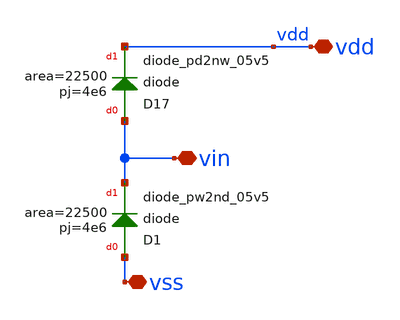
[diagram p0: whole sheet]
** sch_path: xschem/src/ESD/ESD.sch
**.subckt ESD vdd vin vss
*.iopin vdd
*.iopin vin
*.iopin vss
XD17 vin vdd sky130_fd_pr__diode_pd2nw_05v5 area=22500 pj=4e6
XD1 vss vin sky130_fd_pr__diode_pw2nd_05v5 area=22500 pj=4e6
**.ends
.end
